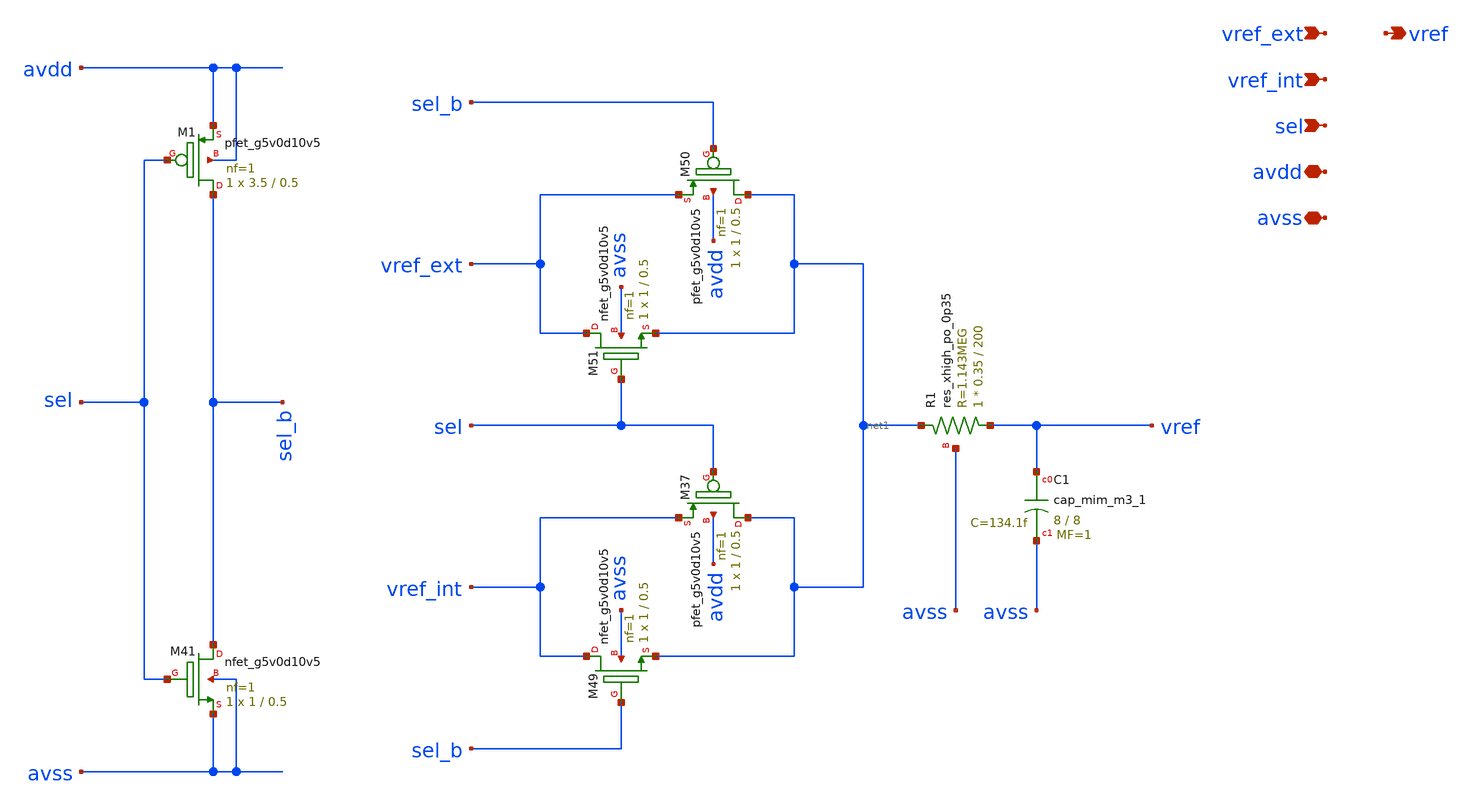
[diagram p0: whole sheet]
** sch_path: xschem/mux21_03v3.sch
**.subckt mux21_03v3 avdd avss sel vref vref_int vref_ext
*.iopin avdd
*.iopin avss
*.ipin sel
*.opin vref
*.ipin vref_int
*.ipin vref_ext
XM37 net1 sel vref_int avdd sky130_fd_pr__pfet_g5v0d10v5 L=0.5 W=1 nf=1 ad='int((nf+1)/2) * W/nf * 0.29'
+ as='int((nf+2)/2) * W/nf * 0.29' pd='2*int((nf+1)/2) * (W/nf + 0.29)' ps='2*int((nf+2)/2) * (W/nf + 0.29)'
+ nrd='0.29 / W' nrs='0.29 / W' sa=0 sb=0 sd=0 mult=1 m=1
XM49 vref_int sel_b net1 avss sky130_fd_pr__nfet_g5v0d10v5 L=0.5 W=1 nf=1 ad='int((nf+1)/2) * W/nf * 0.29'
+ as='int((nf+2)/2) * W/nf * 0.29' pd='2*int((nf+1)/2) * (W/nf + 0.29)' ps='2*int((nf+2)/2) * (W/nf + 0.29)'
+ nrd='0.29 / W' nrs='0.29 / W' sa=0 sb=0 sd=0 mult=1 m=1
XM50 net1 sel_b vref_ext avdd sky130_fd_pr__pfet_g5v0d10v5 L=0.5 W=1 nf=1 ad='int((nf+1)/2) * W/nf * 0.29'
+ as='int((nf+2)/2) * W/nf * 0.29' pd='2*int((nf+1)/2) * (W/nf + 0.29)' ps='2*int((nf+2)/2) * (W/nf + 0.29)'
+ nrd='0.29 / W' nrs='0.29 / W' sa=0 sb=0 sd=0 mult=1 m=1
XM51 vref_ext sel net1 avss sky130_fd_pr__nfet_g5v0d10v5 L=0.5 W=1 nf=1 ad='int((nf+1)/2) * W/nf * 0.29'
+ as='int((nf+2)/2) * W/nf * 0.29' pd='2*int((nf+1)/2) * (W/nf + 0.29)' ps='2*int((nf+2)/2) * (W/nf + 0.29)'
+ nrd='0.29 / W' nrs='0.29 / W' sa=0 sb=0 sd=0 mult=1 m=1
XM1 sel_b sel avdd avdd sky130_fd_pr__pfet_g5v0d10v5 L=0.5 W=3.5 nf=1 ad='int((nf+1)/2) * W/nf * 0.29'
+ as='int((nf+2)/2) * W/nf * 0.29' pd='2*int((nf+1)/2) * (W/nf + 0.29)' ps='2*int((nf+2)/2) * (W/nf + 0.29)'
+ nrd='0.29 / W' nrs='0.29 / W' sa=0 sb=0 sd=0 mult=1 m=1
XM41 sel_b sel avss avss sky130_fd_pr__nfet_g5v0d10v5 L=0.5 W=1 nf=1 ad='int((nf+1)/2) * W/nf * 0.29'
+ as='int((nf+2)/2) * W/nf * 0.29' pd='2*int((nf+1)/2) * (W/nf + 0.29)' ps='2*int((nf+2)/2) * (W/nf + 0.29)'
+ nrd='0.29 / W' nrs='0.29 / W' sa=0 sb=0 sd=0 mult=1 m=1
XC1 vref avss sky130_fd_pr__cap_mim_m3_1 W=8 L=8 MF=1 m=1
XR1 vref net1 avss sky130_fd_pr__res_xhigh_po_0p35 L=200 mult=1 m=1
**.ends
.end
